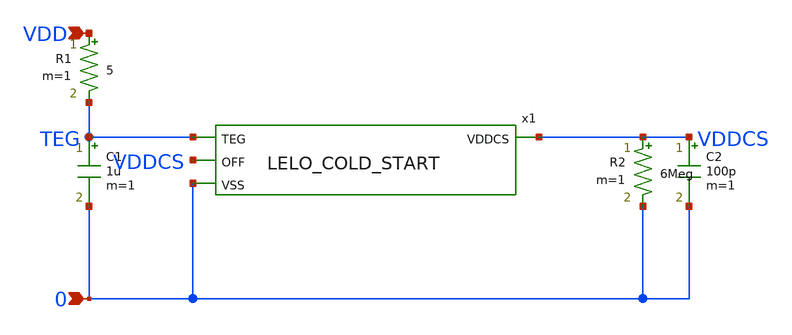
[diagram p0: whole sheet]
** sch_path: design/LELO_SVOD_SKY130A/LELO_COLD_START_TB.sch
**.subckt LELO_COLD_START_TB VDD 0
*.ipin VDD
*.ipin 0
x1 TEG VDDCS VDDCS 0 LELO_COLD_START
R1 VDD TEG 5 m=1
C1 TEG 0 1u m=1
C2 VDDCS 0 100p m=1
R2 VDDCS 0 6Meg m=1
**.ends

* expanding   symbol:  LELO_SVOD_SKY130A/LELO_COLD_START.sym # of pins=4
** sym_path: design/LELO_SVOD_SKY130A/LELO_COLD_START.sym
** sch_path: design/LELO_SVOD_SKY130A/LELO_COLD_START.sch
.subckt LELO_COLD_START TEG VDDCS OFF VSS
*.ipin VSS
*.ipin TEG
*.opin VDDCS
*.ipin OFF
XM1 net1 VG2 net5 VSS sky130_fd_pr__nfet_20v0_zvt W=60 L=0.5 m=91
XM2 net2 VG1 net5 VSS sky130_fd_pr__nfet_20v0_zvt W=60 L=0.5 m=91
XM3 TEG TEG net3 TEG sky130_fd_pr__nfet_01v8_lvt L=0.15 W=8 nf=1 ad='int((1 + 1)/2) * 8 / 1 * 0.29' as='int((1 + 2)/2) * 8 / 1 * 0.29'
+ pd='2*int((1 + 1)/2) * (8 / 1 + 0.29)' ps='2*int((1 + 2)/2) * (8 / 1 + 0.29)' nrd='0.29 / 8 ' nrs='0.29 / 8 '
+ sa=0 sb=0 sd=0 mult=1 m=1
XM7 net3 net3 net4 net3 sky130_fd_pr__nfet_01v8_lvt L=0.15 W=8 nf=1 ad='int((1 + 1)/2) * 8 / 1 * 0.29'
+ as='int((1 + 2)/2) * 8 / 1 * 0.29' pd='2*int((1 + 1)/2) * (8 / 1 + 0.29)' ps='2*int((1 + 2)/2) * (8 / 1 + 0.29)'
+ nrd='0.29 / 8 ' nrs='0.29 / 8 ' sa=0 sb=0 sd=0 mult=1 m=1
XM8 net4 net4 VDDCS net4 sky130_fd_pr__nfet_01v8_lvt L=0.15 W=8 nf=1 ad='int((1 + 1)/2) * 8 / 1 * 0.29'
+ as='int((1 + 2)/2) * 8 / 1 * 0.29' pd='2*int((1 + 1)/2) * (8 / 1 + 0.29)' ps='2*int((1 + 2)/2) * (8 / 1 + 0.29)'
+ nrd='0.29 / 8 ' nrs='0.29 / 8 ' sa=0 sb=0 sd=0 mult=1 m=1
XM4 net5 OFF VSS VSS sky130_fd_pr__nfet_20v0_zvt W=60 L=0.5 m=200
x3 net1 VG1 1812PS-474_imp
x4 VG2 net2 1812PS-474_imp
x1 TEG net1 1812PS-562_imp
x2 TEG net2 1812PS-562_imp
C1 net3 VG1 1p m=1
C2 net4 VG2 1p m=1
.ends


* expanding   symbol:  LELO_SVOD_SKY130A/1812PS-474_imp.sym # of pins=2
** sym_path: design/LELO_SVOD_SKY130A/1812PS-474_imp.sym

.subckt 1812PS-474_imp port1 port2
X1 port1 port2 Model1D R1=105 R2=5.9 C= 3.15p K1=1E-06 K2=108.9 K3= 470u K4=0.000001 K5=0.000001 L=0
+ Is=0 a=0 L_Z0=0 L_EL=0 L_F0=0E6 PkZ=191622.479
.ends 1812PS-474_imp

* expanding   symbol:  LELO_SVOD_SKY130A/1812PS-562_imp.sym # of pins=2
** sym_path: design/LELO_SVOD_SKY130A/1812PS-562_imp.sym

.subckt 1812PS-562_imp port1 port2
X1 port1 port2 Model1D R1=22 R2=0.12 C= 0.289p K1=0.000001 K2=0.494 K3= 5.6u K4=0.00145 K5=0.0000514
+ L=0 Is=0 a=0 L_Z0=0 L_EL=0 L_F0=0E6 PkZ=5489.2717
.ends 1812PS-562_imp
.end
